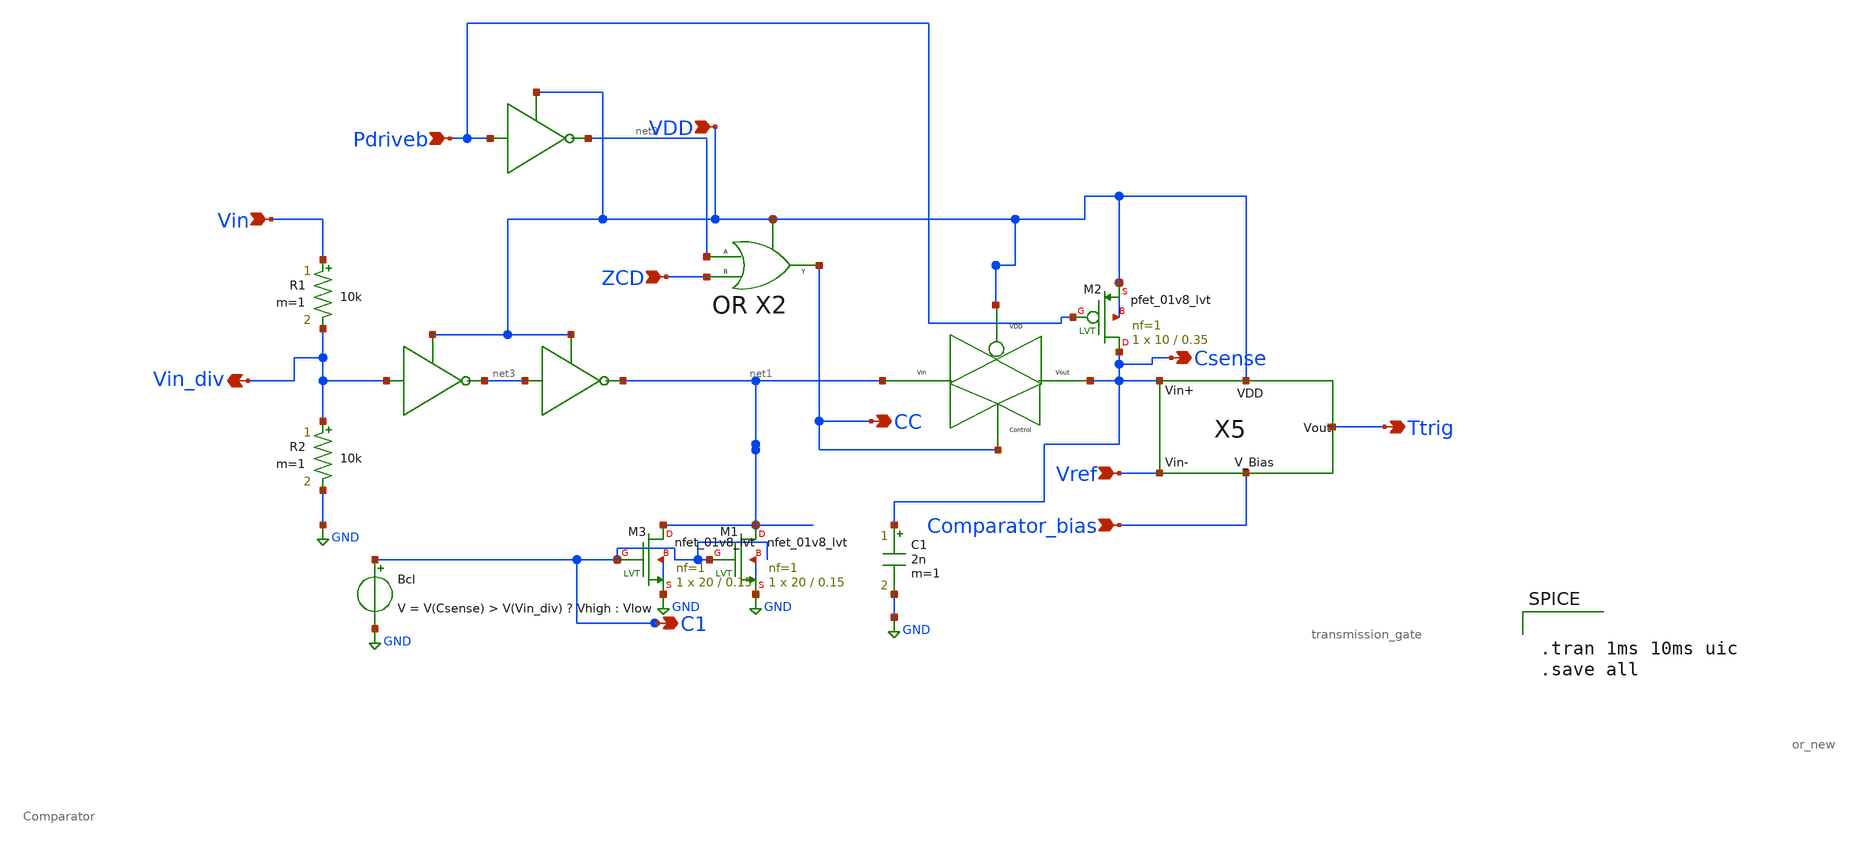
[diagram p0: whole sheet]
** sch_path: Current Sensor/otg.sch
**.subckt otg Vref Vin_div Comparator_bias Pdriveb ZCD Vin Ttrig VDD Csense C1 CC
*.ipin Vref
*.opin Vin_div
*.ipin Comparator_bias
*.ipin Pdriveb
*.ipin ZCD
*.ipin Vin
*.opin Ttrig
*.ipin VDD
*.opin Csense
*.opin C1
*.opin CC
X1 net1 Csense CC VDD transmission_gate
X5 Comparator_bias Csense Vref Ttrig VDD Comparator
C1 Csense GND 2n m=1
X2 ZCD net2 CC VDD or_new
XM1 net1 C1 GND GND sky130_fd_pr__nfet_01v8_lvt L=0.15 W=20 nf=1 ad='int((nf+1)/2) * W/nf * 0.29' as='int((nf+2)/2) * W/nf * 0.29'
+ pd='2*int((nf+1)/2) * (W/nf + 0.29)' ps='2*int((nf+2)/2) * (W/nf + 0.29)' nrd='0.29 / W' nrs='0.29 / W'
+ sa=0 sb=0 sd=0 mult=1 m=1
Bcl C1 GND V = V(Csense) > V(Vin_div) ? Vhigh : Vlow
R1 Vin Vin_div 10k m=1
R2 Vin_div GND 10k m=1
XM3 net1 C1 GND GND sky130_fd_pr__nfet_01v8_lvt L=0.15 W=20 nf=1 ad='int((nf+1)/2) * W/nf * 0.29' as='int((nf+2)/2) * W/nf * 0.29'
+ pd='2*int((nf+1)/2) * (W/nf + 0.29)' ps='2*int((nf+2)/2) * (W/nf + 0.29)' nrd='0.29 / W' nrs='0.29 / W'
+ sa=0 sb=0 sd=0 mult=1 m=1
XM2 Csense Pdriveb VDD VDD sky130_fd_pr__pfet_01v8_lvt L=0.35 W=10 nf=1 ad='int((nf+1)/2) * W/nf * 0.29'
+ as='int((nf+2)/2) * W/nf * 0.29' pd='2*int((nf+1)/2) * (W/nf + 0.29)' ps='2*int((nf+2)/2) * (W/nf + 0.29)'
+ nrd='0.29 / W' nrs='0.29 / W' sa=0 sb=0 sd=0 mult=1 m=1
**** begin user architecture code


.tran 1ms 10ms uic
.save all


** opencircuitdesign pdks install
.lib $::SKYWATER_MODELS/sky130.lib.spice tt_mm


**** end user architecture code
**.ends
.GLOBAL GND
.end
